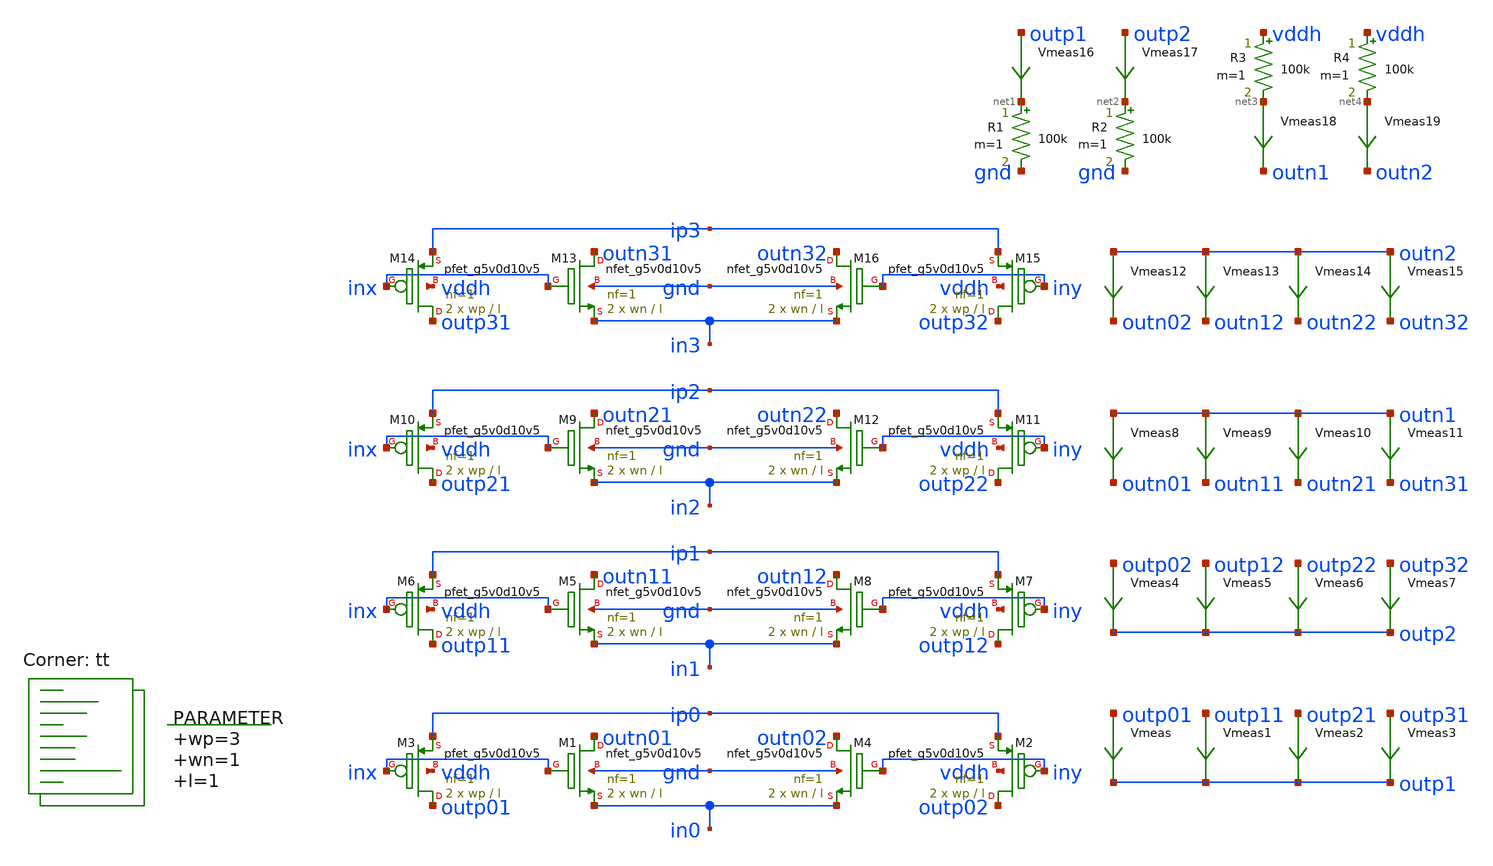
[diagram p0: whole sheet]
** sch_path: xschem/op_amp_input_stage.sch
**.subckt op_amp_input_stage
XM1 outn01 inx in0 gnd sky130_fd_pr__nfet_g5v0d10v5 L=l W=wn nf=1 ad='int((nf+1)/2) * W/nf * 0.29' as='int((nf+2)/2) * W/nf * 0.29'
+ pd='2*int((nf+1)/2) * (W/nf + 0.29)' ps='2*int((nf+2)/2) * (W/nf + 0.29)' nrd='0.29 / W' nrs='0.29 / W'
+ sa=0 sb=0 sd=0 mult=2 m=2
Vmeas outp01 outp1 0
.save i(vmeas)
XM3 outp01 inx ip0 vddh sky130_fd_pr__pfet_g5v0d10v5 L=l W=wp nf=1 ad='int((nf+1)/2) * W/nf * 0.29' as='int((nf+2)/2) * W/nf * 0.29'
+ pd='2*int((nf+1)/2) * (W/nf + 0.29)' ps='2*int((nf+2)/2) * (W/nf + 0.29)' nrd='0.29 / W' nrs='0.29 / W'
+ sa=0 sb=0 sd=0 mult=2 m=2
R1 net1 gnd 100k m=1
.param wp=3 wn=1 l=1
XM2 outp02 iny ip0 vddh sky130_fd_pr__pfet_g5v0d10v5 L=l W=wp nf=1 ad='int((nf+1)/2) * W/nf * 0.29' as='int((nf+2)/2) * W/nf * 0.29'
+ pd='2*int((nf+1)/2) * (W/nf + 0.29)' ps='2*int((nf+2)/2) * (W/nf + 0.29)' nrd='0.29 / W' nrs='0.29 / W'
+ sa=0 sb=0 sd=0 mult=2 m=2
XM4 outn02 iny in0 gnd sky130_fd_pr__nfet_g5v0d10v5 L=l W=wn nf=1 ad='int((nf+1)/2) * W/nf * 0.29' as='int((nf+2)/2) * W/nf * 0.29'
+ pd='2*int((nf+1)/2) * (W/nf + 0.29)' ps='2*int((nf+2)/2) * (W/nf + 0.29)' nrd='0.29 / W' nrs='0.29 / W'
+ sa=0 sb=0 sd=0 mult=2 m=2
XM5 outn11 inx in1 gnd sky130_fd_pr__nfet_g5v0d10v5 L=l W=wn nf=1 ad='int((nf+1)/2) * W/nf * 0.29' as='int((nf+2)/2) * W/nf * 0.29'
+ pd='2*int((nf+1)/2) * (W/nf + 0.29)' ps='2*int((nf+2)/2) * (W/nf + 0.29)' nrd='0.29 / W' nrs='0.29 / W'
+ sa=0 sb=0 sd=0 mult=2 m=2
XM6 outp11 inx ip1 vddh sky130_fd_pr__pfet_g5v0d10v5 L=l W=wp nf=1 ad='int((nf+1)/2) * W/nf * 0.29' as='int((nf+2)/2) * W/nf * 0.29'
+ pd='2*int((nf+1)/2) * (W/nf + 0.29)' ps='2*int((nf+2)/2) * (W/nf + 0.29)' nrd='0.29 / W' nrs='0.29 / W'
+ sa=0 sb=0 sd=0 mult=2 m=2
XM7 outp12 iny ip1 vddh sky130_fd_pr__pfet_g5v0d10v5 L=l W=wp nf=1 ad='int((nf+1)/2) * W/nf * 0.29' as='int((nf+2)/2) * W/nf * 0.29'
+ pd='2*int((nf+1)/2) * (W/nf + 0.29)' ps='2*int((nf+2)/2) * (W/nf + 0.29)' nrd='0.29 / W' nrs='0.29 / W'
+ sa=0 sb=0 sd=0 mult=2 m=2
XM8 outn12 iny in1 gnd sky130_fd_pr__nfet_g5v0d10v5 L=l W=wn nf=1 ad='int((nf+1)/2) * W/nf * 0.29' as='int((nf+2)/2) * W/nf * 0.29'
+ pd='2*int((nf+1)/2) * (W/nf + 0.29)' ps='2*int((nf+2)/2) * (W/nf + 0.29)' nrd='0.29 / W' nrs='0.29 / W'
+ sa=0 sb=0 sd=0 mult=2 m=2
XM9 outn21 inx in2 gnd sky130_fd_pr__nfet_g5v0d10v5 L=l W=wn nf=1 ad='int((nf+1)/2) * W/nf * 0.29' as='int((nf+2)/2) * W/nf * 0.29'
+ pd='2*int((nf+1)/2) * (W/nf + 0.29)' ps='2*int((nf+2)/2) * (W/nf + 0.29)' nrd='0.29 / W' nrs='0.29 / W'
+ sa=0 sb=0 sd=0 mult=2 m=2
XM10 outp21 inx ip2 vddh sky130_fd_pr__pfet_g5v0d10v5 L=l W=wp nf=1 ad='int((nf+1)/2) * W/nf * 0.29'
+ as='int((nf+2)/2) * W/nf * 0.29' pd='2*int((nf+1)/2) * (W/nf + 0.29)' ps='2*int((nf+2)/2) * (W/nf + 0.29)'
+ nrd='0.29 / W' nrs='0.29 / W' sa=0 sb=0 sd=0 mult=2 m=2
XM11 outp22 iny ip2 vddh sky130_fd_pr__pfet_g5v0d10v5 L=l W=wp nf=1 ad='int((nf+1)/2) * W/nf * 0.29'
+ as='int((nf+2)/2) * W/nf * 0.29' pd='2*int((nf+1)/2) * (W/nf + 0.29)' ps='2*int((nf+2)/2) * (W/nf + 0.29)'
+ nrd='0.29 / W' nrs='0.29 / W' sa=0 sb=0 sd=0 mult=2 m=2
XM12 outn22 iny in2 gnd sky130_fd_pr__nfet_g5v0d10v5 L=l W=wn nf=1 ad='int((nf+1)/2) * W/nf * 0.29' as='int((nf+2)/2) * W/nf * 0.29'
+ pd='2*int((nf+1)/2) * (W/nf + 0.29)' ps='2*int((nf+2)/2) * (W/nf + 0.29)' nrd='0.29 / W' nrs='0.29 / W'
+ sa=0 sb=0 sd=0 mult=2 m=2
XM13 outn31 inx in3 gnd sky130_fd_pr__nfet_g5v0d10v5 L=l W=wn nf=1 ad='int((nf+1)/2) * W/nf * 0.29' as='int((nf+2)/2) * W/nf * 0.29'
+ pd='2*int((nf+1)/2) * (W/nf + 0.29)' ps='2*int((nf+2)/2) * (W/nf + 0.29)' nrd='0.29 / W' nrs='0.29 / W'
+ sa=0 sb=0 sd=0 mult=2 m=2
XM14 outp31 inx ip3 vddh sky130_fd_pr__pfet_g5v0d10v5 L=l W=wp nf=1 ad='int((nf+1)/2) * W/nf * 0.29'
+ as='int((nf+2)/2) * W/nf * 0.29' pd='2*int((nf+1)/2) * (W/nf + 0.29)' ps='2*int((nf+2)/2) * (W/nf + 0.29)'
+ nrd='0.29 / W' nrs='0.29 / W' sa=0 sb=0 sd=0 mult=2 m=2
XM15 outp32 iny ip3 vddh sky130_fd_pr__pfet_g5v0d10v5 L=l W=wp nf=1 ad='int((nf+1)/2) * W/nf * 0.29'
+ as='int((nf+2)/2) * W/nf * 0.29' pd='2*int((nf+1)/2) * (W/nf + 0.29)' ps='2*int((nf+2)/2) * (W/nf + 0.29)'
+ nrd='0.29 / W' nrs='0.29 / W' sa=0 sb=0 sd=0 mult=2 m=2
XM16 outn32 iny in3 gnd sky130_fd_pr__nfet_g5v0d10v5 L=l W=wn nf=1 ad='int((nf+1)/2) * W/nf * 0.29' as='int((nf+2)/2) * W/nf * 0.29'
+ pd='2*int((nf+1)/2) * (W/nf + 0.29)' ps='2*int((nf+2)/2) * (W/nf + 0.29)' nrd='0.29 / W' nrs='0.29 / W'
+ sa=0 sb=0 sd=0 mult=2 m=2
Vmeas1 outp11 outp1 0
.save i(vmeas1)
Vmeas2 outp21 outp1 0
.save i(vmeas2)
Vmeas3 outp31 outp1 0
.save i(vmeas3)
Vmeas4 outp02 outp2 0
.save i(vmeas4)
R2 net2 gnd 100k m=1
Vmeas5 outp12 outp2 0
.save i(vmeas5)
Vmeas6 outp22 outp2 0
.save i(vmeas6)
Vmeas7 outp32 outp2 0
.save i(vmeas7)
Vmeas8 outn1 outn01 0
.save i(vmeas8)
R3 vddh net3 100k m=1
Vmeas9 outn1 outn11 0
.save i(vmeas9)
Vmeas10 outn1 outn21 0
.save i(vmeas10)
Vmeas11 outn1 outn31 0
.save i(vmeas11)
Vmeas12 outn2 outn02 0
.save i(vmeas12)
R4 vddh net4 100k m=1
Vmeas13 outn2 outn12 0
.save i(vmeas13)
Vmeas14 outn2 outn22 0
.save i(vmeas14)
Vmeas15 outn2 outn32 0
.save i(vmeas15)
Vmeas16 outp1 net1 0
.save i(vmeas16)
Vmeas17 outp2 net2 0
.save i(vmeas17)
Vmeas18 net3 outn1 0
.save i(vmeas18)
Vmeas19 net4 outn2 0
.save i(vmeas19)
**** begin user architecture code
.lib $::SKYWATER_MODELS/sky130.lib.spice tt



  .option wnflag=1
  .option safecurrents
  ********************Static Current Sources***************************
  .param base_current=100n
  .param i0=base_current i1={2*i0} i2={4*i0} i3={8*i0}
  Ip0 vddh ip0 i0
  In0 in0  gnd i0

  Ip1 vddh ip1 i1
  In1 in1  gnd i1

  Ip2 vddh ip2 i2
  In2 in2  gnd i2

  Ip3 vddh ip3 i3
  In3 in3  gnd i3
  ********************Static Voltage Sources***************************
  .param vh=5.5 vcm={vh/2} va={vh/2}
  Vddh vddh gnd dc 5.

  vinx inx gnd sin({vcm} {va} 100k)
  viny iny gnd sin({vcm} {-va} 100k)
  ********************Dynamic Voltage Sources***************************
  *******Calculation**********
  .param base_f=100e3 base_t={1/base_f} base_th={base_t/2} base_d={base_th}
  .param d2_th ={base_th} d2_t={2*d2_th}
  .param d1_th ={4*d2_th} d1_t={d0_th}
  .param d0_th ={4*d1_th} d0_t={4*d0_th}

  .param d20_d ={0} d21_d={1*d2_th} d22_d={2*d2_th} d23_d={3*d2_th}
  .param d10_d ={0} d11_d={1*d1_th} d12_d={2*d1_th} d13_d={3*d1_th}
  .param d00_d ={0} d01_d={1*d0_th} d02_d={2*d0_th} d03_d={3*d0_th}
  *******Signals**********
  .param vhi=5.5
*  Vin1 b[0] gnd pulse(0 {vhi} {0} 1p 1p {10u} {20u})
*  Vin2 b[1] gnd pulse(0 {vhi} {0} 1p 1p {20u} {40u})
  ********************Simulation Commands*****************************
  .control
     reset
     save all
     tran 1n 30u
     *dc vin 0 5.5 0.001
     write input_stage-tb.raw
     set appendwrite
*    quit 0
  .endc



**** end user architecture code
**.ends
.end
